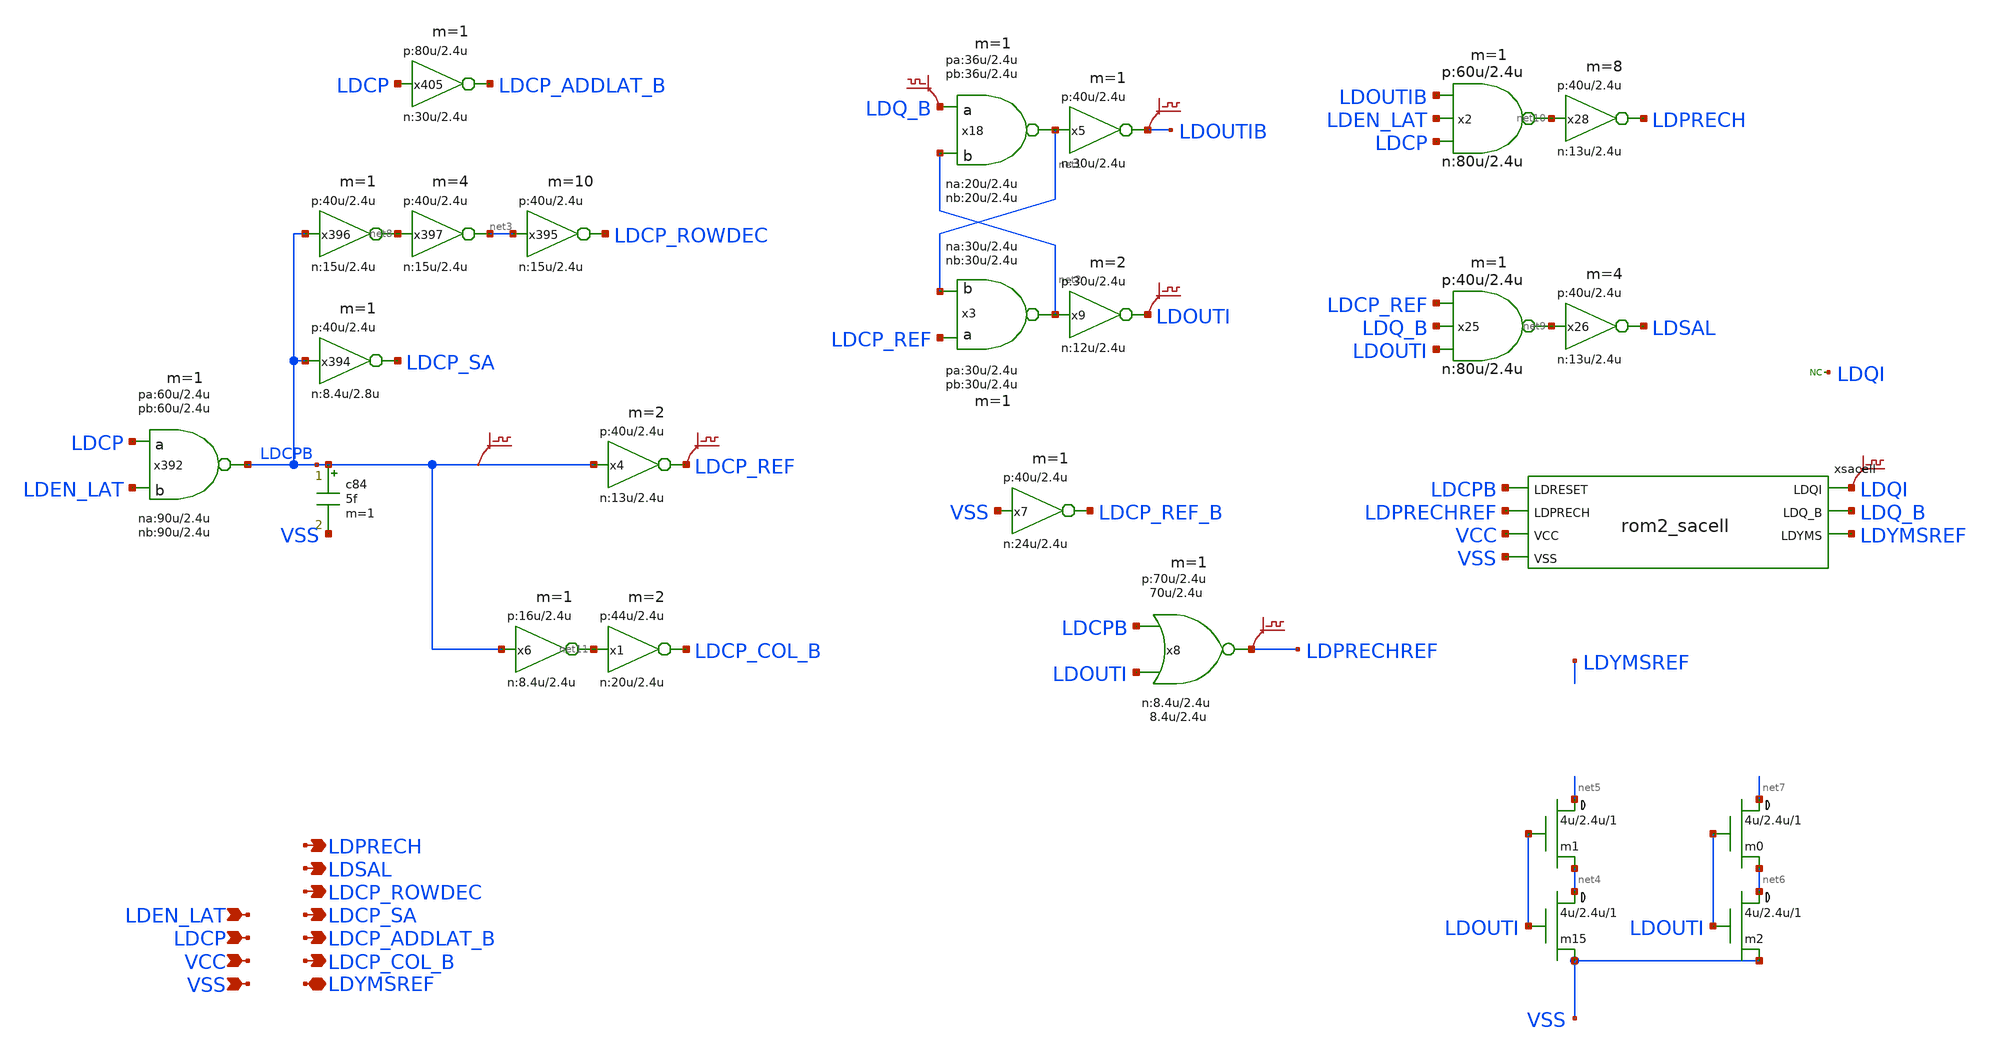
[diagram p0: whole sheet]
** sch_path: xschem_library_oa/rom8k/rom2_ctrl/schematic/rom2_ctrl.sch
* Copyright (C) 1998-2024 Stefan Frederik Schippers
* This program is free software; you can redistribute it and/or modify
* it under the terms of the GNU General Public License as published by
* the Free Software Foundation; either version 2 of the License, or
* (at your option) any later version.
* This program is distributed in the hope that it will be useful,
* but WITHOUT ANY WARRANTY; without even the implied warranty of
* MERCHANTABILITY or FITNESS FOR A PARTICULAR PURPOSE.  See the
* GNU General Public License for more details.
* You should have received a copy of the GNU General Public License
* along with this program; if not, write to the Free Software
**.subckt rom2_ctrl LDPRECH LDSAL LDCP_ROWDEC LDCP_SA LDCP_ADDLAT_B LDCP_COL_B LDEN_LAT LDCP VCC VSS
*+ LDYMSREF
*.opin LDPRECH
*.opin LDSAL
*.opin LDCP_ROWDEC
*.opin LDCP_SA
*.opin LDCP_ADDLAT_B
*.opin LDCP_COL_B
*.ipin LDEN_LAT
*.ipin LDCP
*.ipin VCC
*.ipin VSS
*.iopin LDYMSREF
c84 LDCPB VSS 5f m=1
x392 LDCPB LDCP LDEN_LAT vcc vss lvnand2 wna=90u lna=2.4u wpa=60u lpa=2.4u wnb=90u lnb=2.4u wpb=60u
+ lpb=2.4u m=1
x394 LDCP_SA LDCPB vcc vss lvnot wn=8.4u lln=2.8u wp=40u lp=2.4u m=1
x395 LDCP_ROWDEC net3 vcc vss lvnot wn=15u lln=2.4u wp=40u lp=2.4u m=10
x396 net8 LDCPB vcc vss lvnot wn=15u lln=2.4u wp=40u lp=2.4u m=1
x397 net3 net8 vcc vss lvnot wn=15u lln=2.4u wp=40u lp=2.4u m=4
x405 LDCP_ADDLAT_B LDCP vcc vss lvnot wn=30u lln=2.4u wp=80u lp=2.4u m=1
x7 LDCP_REF_B VSS vcc vss lvnot wn=24u lln=2.4u wp=40u lp=2.4u m=1
x8 LDPRECHREF LDCPB LDOUTI VCC VSS lvnor2 wna=8.4u lna=2.4u wpa=70u lpa=2.4u wnb=8.4u lnb=2.4u
+ wpb=70u lpb=2.4u m=1
x18 net1 LDQ_B net2 VCC VSS lvnand2 wna=20u lna=2.4u wpa=36u lpa=2.4u wnb=20u lnb=2.4u wpb=36u
+ lpb=2.4u m=1
x3 net2 LDCP_REF net1 VCC VSS lvnand2 wna=30u lna=2.4u wpa=30u lpa=2.4u wnb=30u lnb=2.4u wpb=30u
+ lpb=2.4u m=1
m15 net4 LDOUTI VSS 0 cmosn w=4u l=2.4u ad={4u *4.4u} as={4u *4.4u} pd={4u *2 + 8.8u} ps={4u *2 + 8.8u}
+ m=1
x25 net9 LDCP_REF LDQ_B LDOUTI VCC VSS lvnand3 wn=80u lln=2.4u wp=40u lp=2.4u m=1
x26 LDSAL net9 vcc vss lvnot wn=13u lln=2.4u wp=40u lp=2.4u m=4
x28 LDPRECH net10 vcc vss lvnot wn=13u lln=2.4u wp=40u lp=2.4u m=8
x4 LDCP_REF LDCPB vcc vss lvnot wn=13u lln=2.4u wp=40u lp=2.4u m=2
x1 LDCP_COL_B net11 vcc vss lvnot wn=20u lln=2.4u wp=44u lp=2.4u m=2
x6 net11 LDCPB vcc vss lvnot wn=8.4u lln=2.4u wp=16u lp=2.4u m=1
x5 LDOUTIB net1 vcc vss lvnot wn=30u lln=2.4u wp=40u lp=2.4u m=1
x9 LDOUTI net2 vcc vss lvnot wn=12u lln=2.4u wp=30u lp=2.4u m=2
* noconn LDQI
xsacell LDCPB LDPRECHREF VCC VSS LDQI LDQ_B LDYMSREF rom2_sacell
.save v(ldcp_ref)
.save v(ldprechref)
.save v(ldouti)
.save v(ldoutib)
.save v(ldqi)
.save v(ldq_b)
m1 net5 LDOUTI net4 0 cmosn w=4u l=2.4u ad={4u *4.4u} as={4u *4.4u} pd={4u *2 + 8.8u} ps={4u *2 + 8.8u}
+ m=1
x2 net10 LDOUTIB LDEN_LAT LDCP VCC VSS lvnand3 wn=80u lln=2.4u wp=60u lp=2.4u m=1
m2 net6 LDOUTI VSS 0 cmosn w=4u l=2.4u ad={4u *4.4u} as={4u *4.4u} pd={4u *2 + 8.8u} ps={4u *2 + 8.8u}
+ m=1
m0 net7 LDOUTI net6 0 cmosn w=4u l=2.4u ad={4u *4.4u} as={4u *4.4u} pd={4u *2 + 8.8u} ps={4u *2 + 8.8u}
+ m=1
.save v(ldcpb)
**.ends
.end
